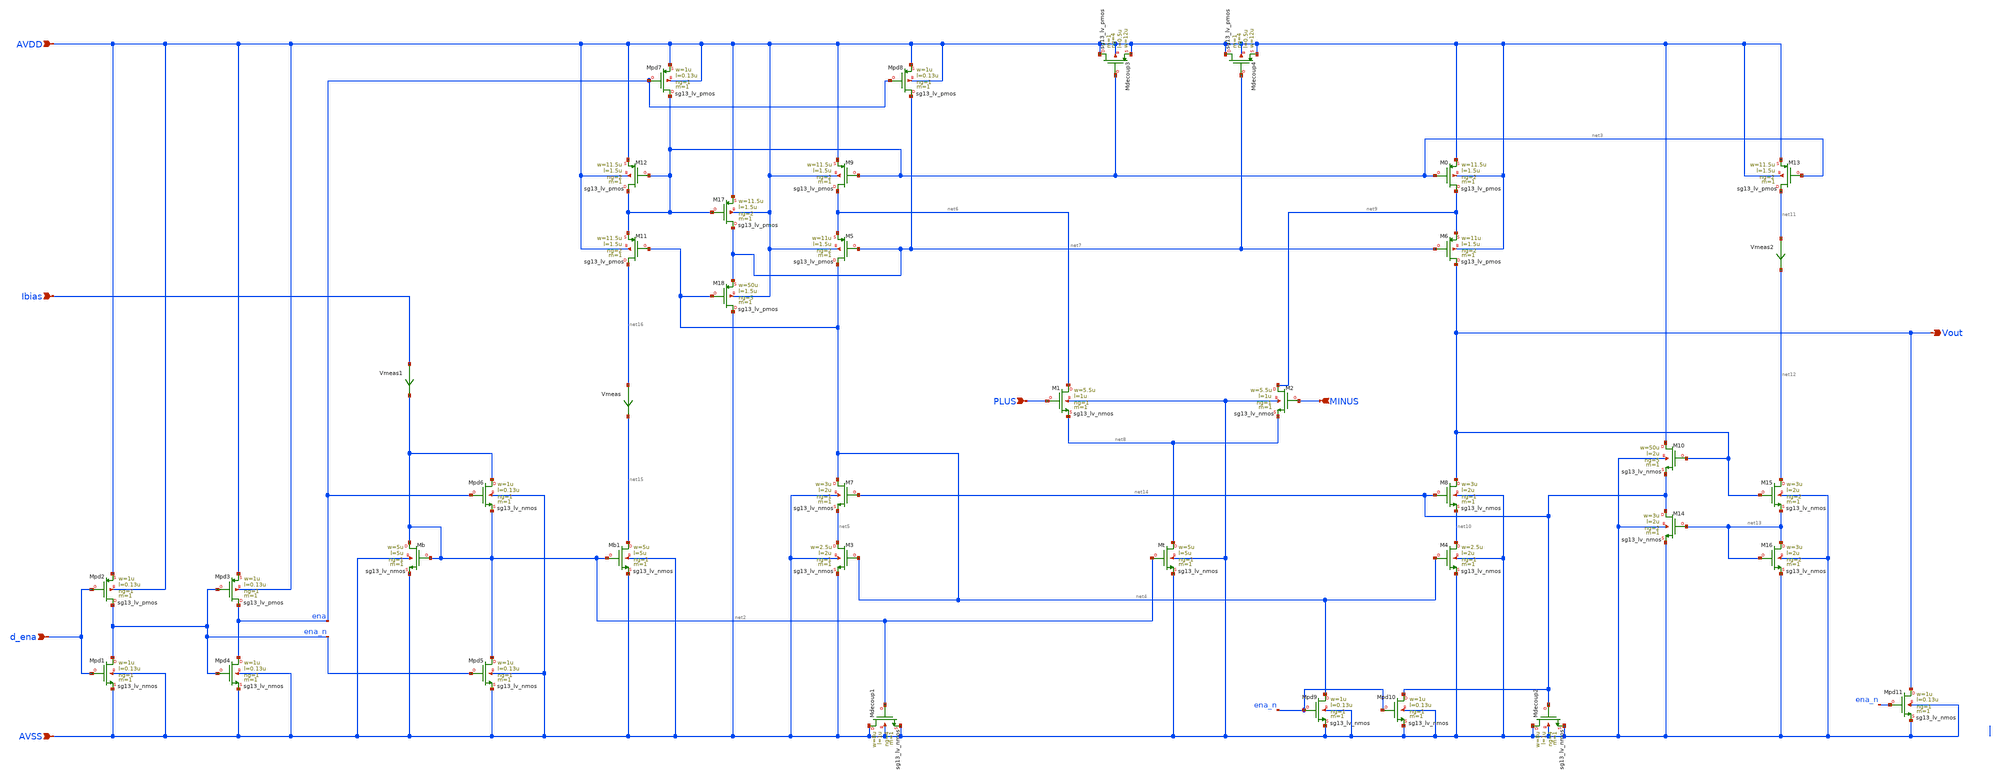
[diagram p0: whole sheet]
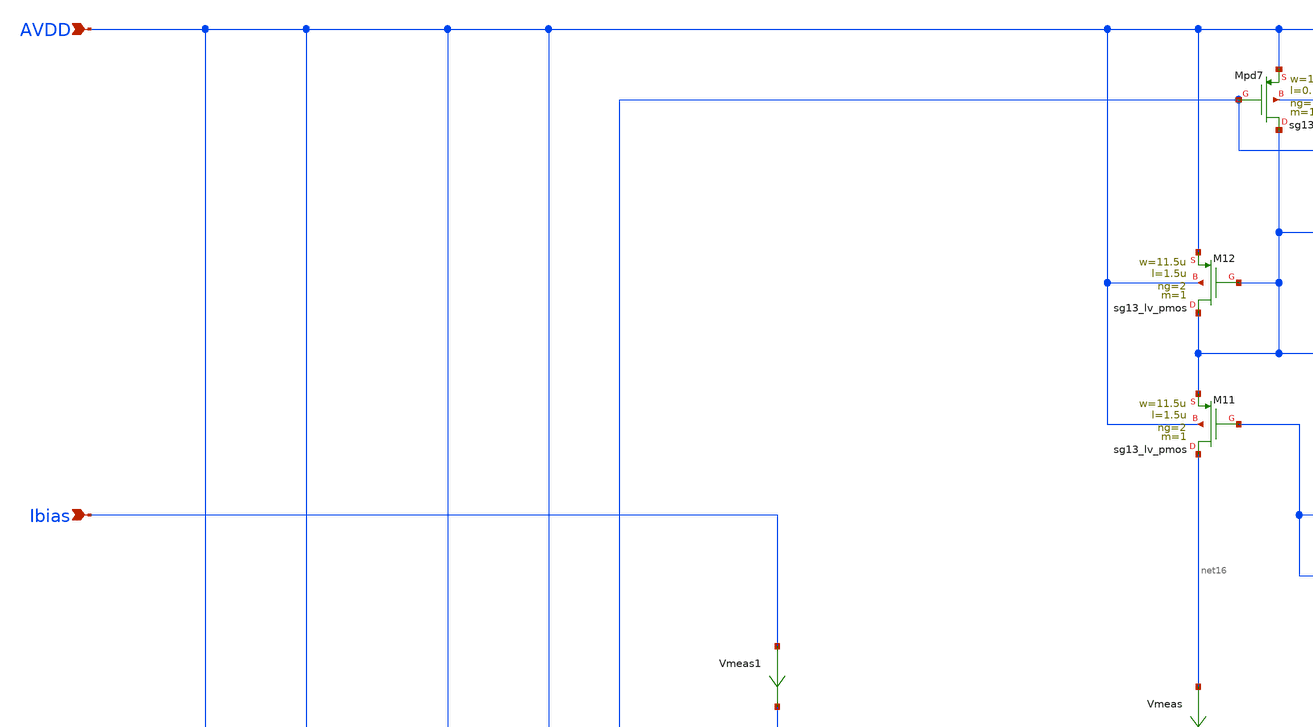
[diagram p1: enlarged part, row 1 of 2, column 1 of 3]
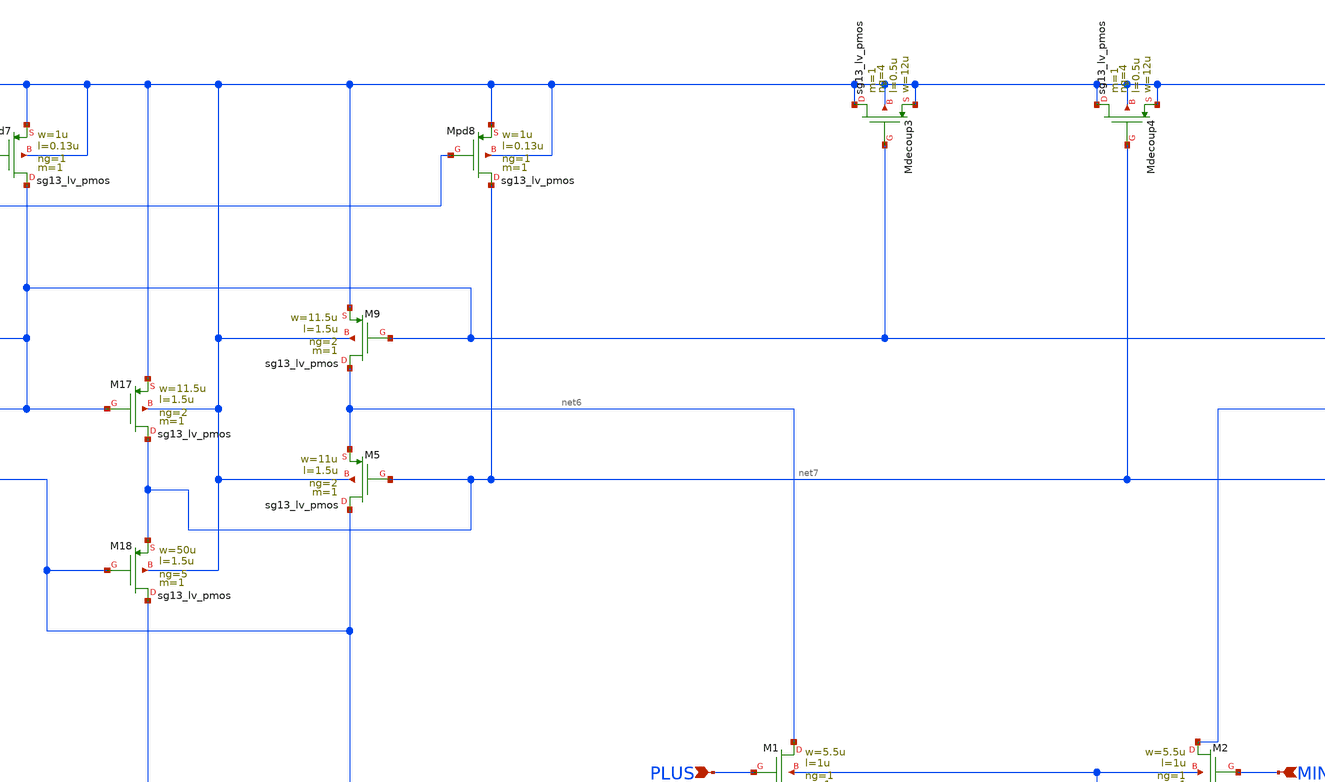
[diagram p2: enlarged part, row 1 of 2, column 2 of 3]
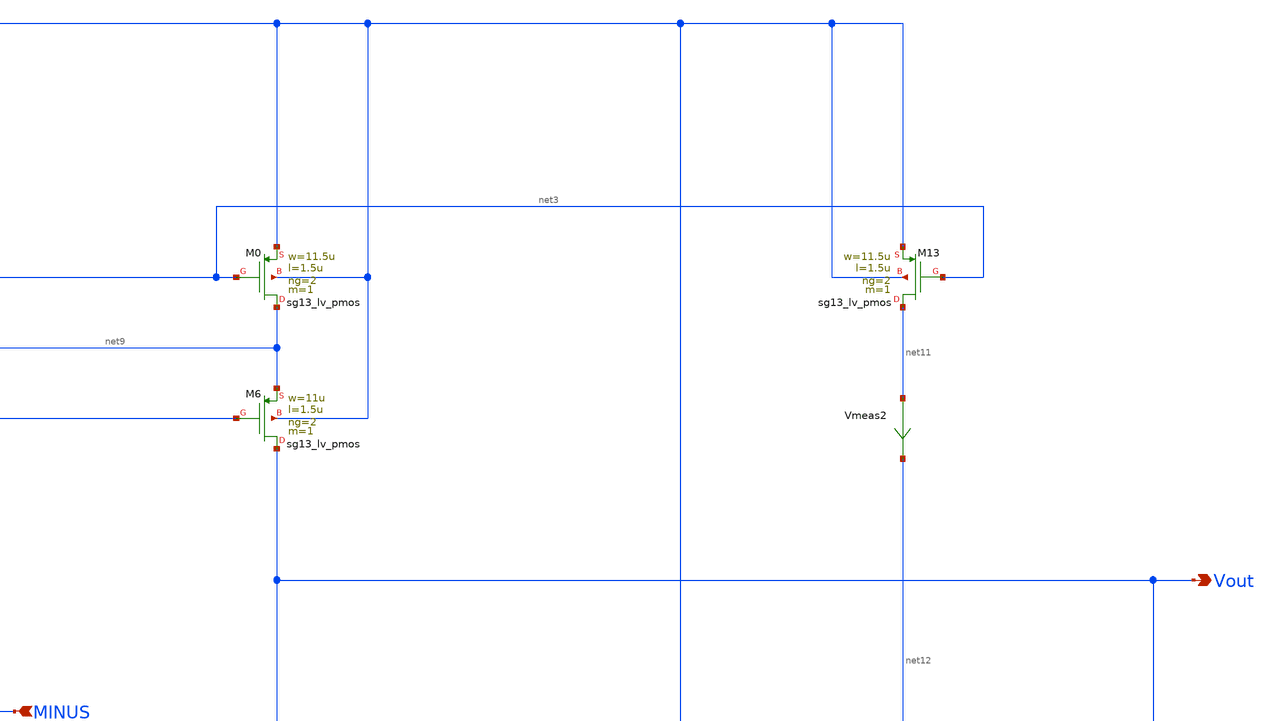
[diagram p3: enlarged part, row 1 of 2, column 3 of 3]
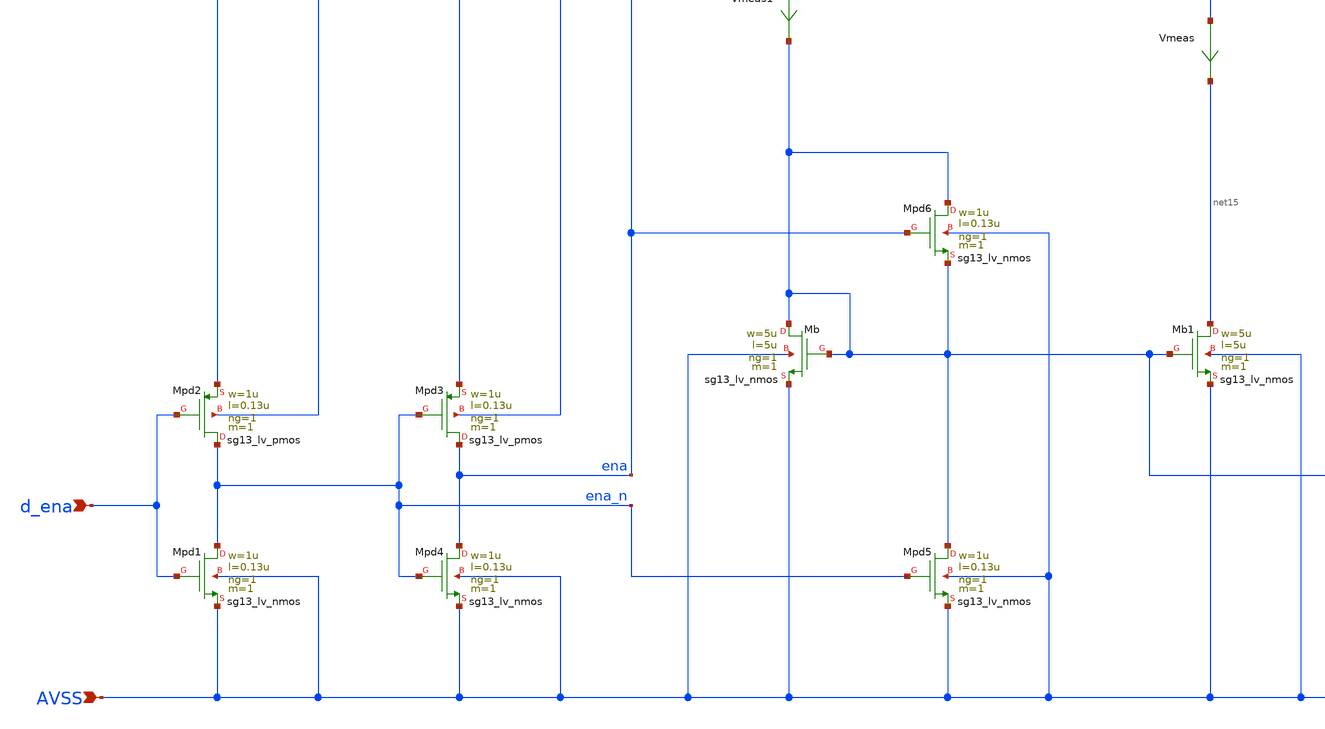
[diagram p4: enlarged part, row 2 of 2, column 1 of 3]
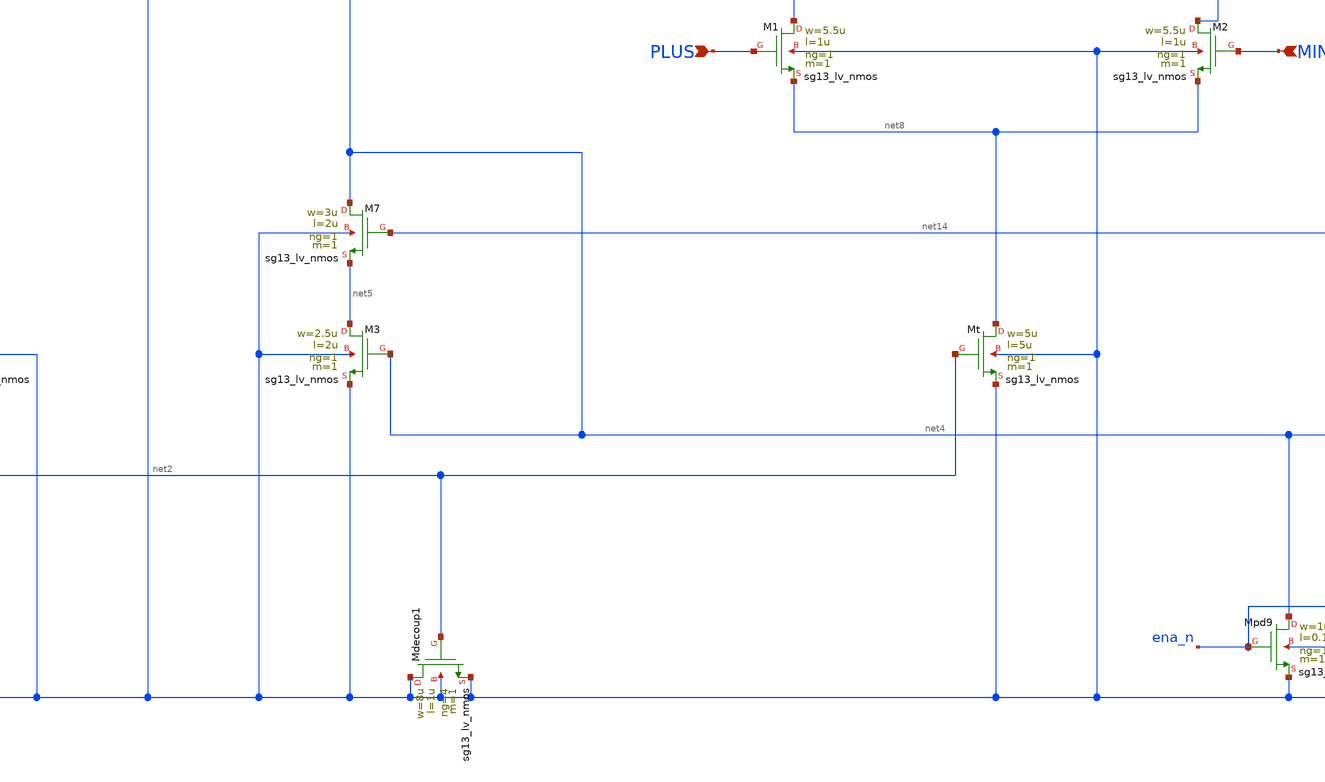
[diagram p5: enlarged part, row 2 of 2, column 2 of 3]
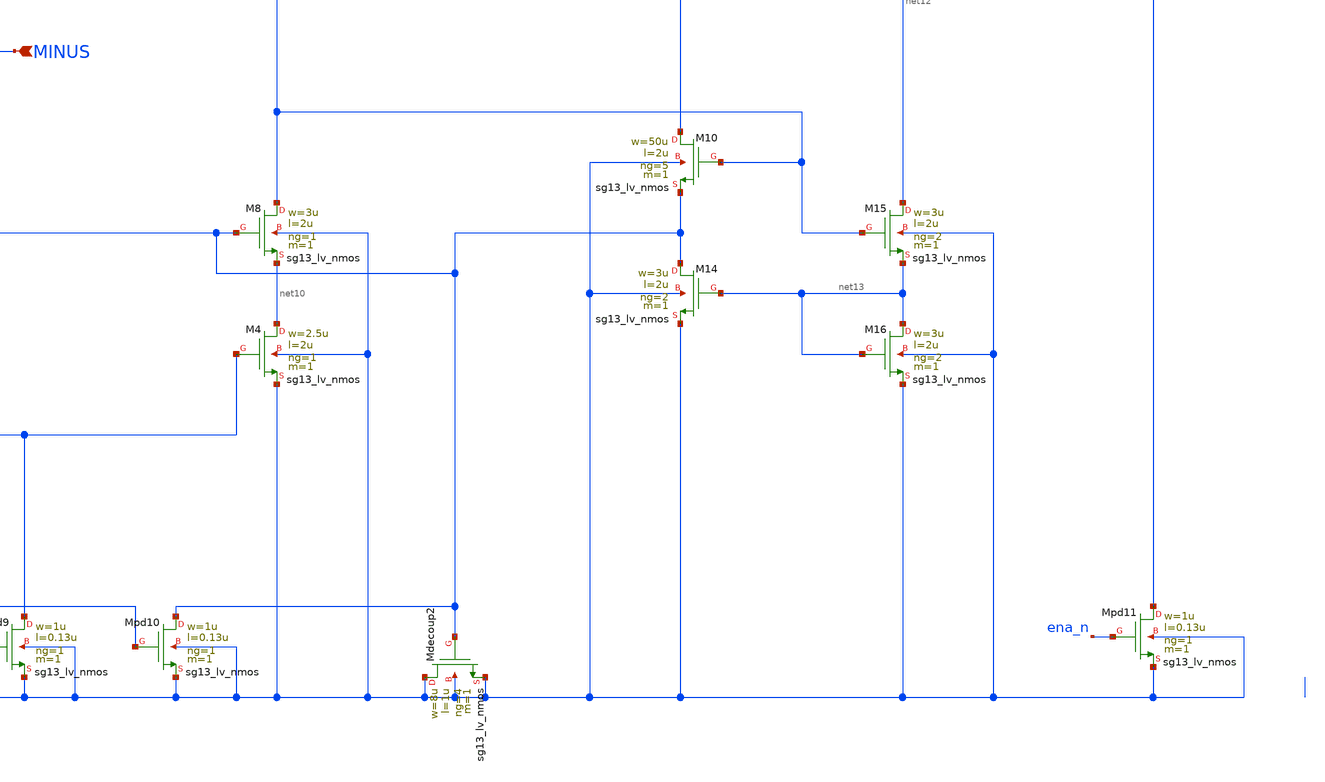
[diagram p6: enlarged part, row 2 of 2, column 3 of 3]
** sch_path: Designs/otas/1_schematics/foldedcascode_nmos_withdummies.sch
* (c) 2025 Thesis_HP, Apache-2.0 license
**.subckt foldedcascode_nmos_withdummies AVSS Ibias AVDD PLUS MINUS Vout d_ena
*.ipin AVSS
*.ipin Ibias
*.ipin AVDD
*.ipin PLUS
*.ipin MINUS
*.opin Vout
*.ipin d_ena
XMpd3 ena ena_n AVDD AVDD sg13_lv_pmos w=1u l=0.13u ng=1 m=1 mm_ok=1
XMpd1 ena_n d_ena AVSS AVSS sg13_lv_nmos w=1u l=0.13u ng=1 m=1 mm_ok=1
XMpd4 ena ena_n AVSS AVSS sg13_lv_nmos w=1u l=0.13u ng=1 m=1 mm_ok=1
XMb net2 net2 AVSS AVSS sg13_lv_nmos w=5u l=5u ng=1 m=1 mm_ok=1
XMpd5 net2 ena_n AVSS AVSS sg13_lv_nmos w=1u l=0.13u ng=1 m=1 mm_ok=1
XMpd6 net2 ena net2 AVSS sg13_lv_nmos w=1u l=0.13u ng=1 m=1 mm_ok=1
XMb1 net15 net2 AVSS AVSS sg13_lv_nmos w=5u l=5u ng=1 m=1 mm_ok=1
Vmeas net16 net15 0
.save i(vmeas)
XM11 net16 net4 net3 AVDD sg13_lv_pmos w=11.5u l=1.5u ng=2 m=1 mm_ok=1
XM12 net3 net3 AVDD AVDD sg13_lv_pmos w=11.5u l=1.5u ng=2 m=1 mm_ok=1
XM18 AVSS net4 net7 AVDD sg13_lv_pmos w=50u l=1.5u ng=5 m=1 mm_ok=1
XM17 net7 net3 AVDD AVDD sg13_lv_pmos w=11.5u l=1.5u ng=2 m=1 mm_ok=1
XM9 net6 net3 AVDD AVDD sg13_lv_pmos w=11.5u l=1.5u ng=2 m=1 mm_ok=1
XM5 net4 net7 net6 AVDD sg13_lv_pmos w=11u l=1.5u ng=2 m=1 mm_ok=1
XM7 net4 net14 net5 AVSS sg13_lv_nmos w=3u l=2u ng=1 m=1 mm_ok=1
XM3 net5 net4 AVSS AVSS sg13_lv_nmos w=2.5u l=2u ng=1 m=1 mm_ok=1
XMpd7 net3 ena AVDD AVDD sg13_lv_pmos w=1u l=0.13u ng=1 m=1 mm_ok=1
XMpd8 net7 ena AVDD AVDD sg13_lv_pmos w=1u l=0.13u ng=1 m=1 mm_ok=1
XMt net8 net2 AVSS AVSS sg13_lv_nmos w=5u l=5u ng=1 m=1 mm_ok=1
XM1 net6 PLUS net8 AVSS sg13_lv_nmos w=5.5u l=1u ng=1 m=1 mm_ok=1
XM2 net9 MINUS net8 AVSS sg13_lv_nmos w=5.5u l=1u ng=1 m=1 mm_ok=1
XM6 Vout net7 net9 AVDD sg13_lv_pmos w=11u l=1.5u ng=2 m=1 mm_ok=1
XM0 net9 net3 AVDD AVDD sg13_lv_pmos w=11.5u l=1.5u ng=2 m=1 mm_ok=1
XMdecoup3 AVDD net3 AVDD AVDD sg13_lv_pmos w=12u l=0.5u ng=4 m=1 mm_ok=1
XMdecoup4 AVDD net7 AVDD AVDD sg13_lv_pmos w=12u l=0.5u ng=4 m=1 mm_ok=1
XM8 Vout net14 net10 AVSS sg13_lv_nmos w=3u l=2u ng=1 m=1 mm_ok=1
XM4 net10 net4 AVSS AVSS sg13_lv_nmos w=2.5u l=2u ng=1 m=1 mm_ok=1
XMdecoup1 AVSS net2 AVSS AVSS sg13_lv_nmos w=8u l=1u ng=4 m=1 mm_ok=1
XM13 net11 net3 AVDD AVDD sg13_lv_pmos w=11.5u l=1.5u ng=2 m=1 mm_ok=1
Vmeas2 net11 net12 0
.save i(vmeas2)
XM15 net12 Vout net13 AVSS sg13_lv_nmos w=3u l=2u ng=2 m=1 mm_ok=1
XM16 net13 net13 AVSS AVSS sg13_lv_nmos w=3u l=2u ng=2 m=1 mm_ok=1
XM14 net14 net13 AVSS AVSS sg13_lv_nmos w=3u l=2u ng=2 m=1 mm_ok=1
XM10 AVDD Vout net14 AVSS sg13_lv_nmos w=50u l=2u ng=5 m=1 mm_ok=1
XMpd11 Vout ena_n AVSS AVSS sg13_lv_nmos w=1u l=0.13u ng=1 m=1 mm_ok=1
XMdecoup2 AVSS net14 AVSS AVSS sg13_lv_nmos w=8u l=1u ng=4 m=1 mm_ok=1
XMpd10 net14 ena_n AVSS AVSS sg13_lv_nmos w=1u l=0.13u ng=1 m=1 mm_ok=1
XMpd9 net4 ena_n AVSS AVSS sg13_lv_nmos w=1u l=0.13u ng=1 m=1 mm_ok=1
XMpd2 ena_n d_ena AVDD AVDD sg13_lv_pmos w=1u l=0.13u ng=1 m=1 mm_ok=1
Vmeas1 Ibias net2 0
.save i(vmeas1)
**.ends
.end
